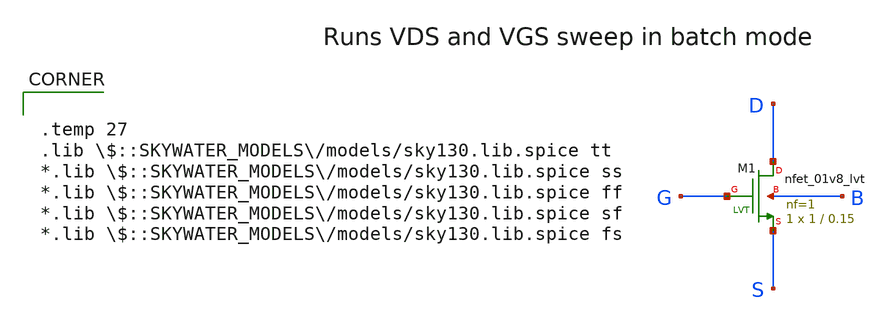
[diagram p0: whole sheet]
** sch_path: nmos_tb.sch
**.subckt nmos_tb
XM1 D G S B sky130_fd_pr__nfet_01v8_lvt L=0.15 W=1 nf=1 ad='int((nf+1)/2) * W/nf * 0.29' as='int((nf+2)/2) * W/nf * 0.29'
+ pd='2*int((nf+1)/2) * (W/nf + 0.29)' ps='2*int((nf+2)/2) * (W/nf + 0.29)' nrd='0.29 / W' nrs='0.29 / W'
+ sa=0 sb=0 sd=0 mult=1 m=1
**** begin user architecture code

.temp 27
.lib $::SKYWATER_MODELS/models/sky130.lib.spice tt
*.lib $::SKYWATER_MODELS/models/sky130.lib.spice ss
*.lib $::SKYWATER_MODELS/models/sky130.lib.spice ff
*.lib $::SKYWATER_MODELS/models/sky130.lib.spice sf
*.lib $::SKYWATER_MODELS/models/sky130.lib.spice fs



Vg G 0 1.8
Vs S 0 0
Vd D 0 1.8
Vb B 0 0

.control

save v(G) v(D) v(S) v(B)
save @m.xm1.msky130_fd_pr__nfet_01v8_lvt[gm]
save @m.xm1.msky130_fd_pr__nfet_01v8_lvt[gmbs]
save @m.xm1.msky130_fd_pr__nfet_01v8_lvt[gds]
save @m.xm1.msky130_fd_pr__nfet_01v8_lvt[vdsat]
save @m.xm1.msky130_fd_pr__nfet_01v8_lvt[vth]
save @m.xm1.msky130_fd_pr__nfet_01v8_lvt[id]
save @m.xm1.msky130_fd_pr__nfet_01v8_lvt[vbs]
save @m.xm1.msky130_fd_pr__nfet_01v8_lvt[vgs]
save @m.xm1.msky130_fd_pr__nfet_01v8_lvt[vds]
save @m.xm1.msky130_fd_pr__nfet_01v8_lvt[cgg]
save @m.xm1.msky130_fd_pr__nfet_01v8_lvt[cgs]
save @m.xm1.msky130_fd_pr__nfet_01v8_lvt[cgd]
save @m.xm1.msky130_fd_pr__nfet_01v8_lvt[cbg]
save @m.xm1.msky130_fd_pr__nfet_01v8_lvt[cbd]
save @m.xm1.msky130_fd_pr__nfet_01v8_lvt[cbs]
save @m.xm1.msky130_fd_pr__nfet_01v8_lvt[cdg]
save @m.xm1.msky130_fd_pr__nfet_01v8_lvt[cdd]
save @m.xm1.msky130_fd_pr__nfet_01v8_lvt[cds]
save @m.xm1.msky130_fd_pr__nfet_01v8_lvt[csg]
save @m.xm1.msky130_fd_pr__nfet_01v8_lvt[csd]
save @m.xm1.msky130_fd_pr__nfet_01v8_lvt[css]
save @m.xm1.msky130_fd_pr__nfet_01v8_lvt[cgb]
save @m.xm1.msky130_fd_pr__nfet_01v8_lvt[cdb]
save @m.xm1.msky130_fd_pr__nfet_01v8_lvt[csb]
save @m.xm1.msky130_fd_pr__nfet_01v8_lvt[cbb]
save @m.xm1.msky130_fd_pr__nfet_01v8_lvt[capbd]
save @m.xm1.msky130_fd_pr__nfet_01v8_lvt[capbs]

*dc Vd 0 1.8 0.1
dc Vd 0 1.8 0.3 Vg 0 1.8 0.3
reshape all [7] ;same value as second sweep length

plot @m.xm1.msky130_fd_pr__nfet_01v8_lvt[id] vs v(d) title 'id vs vd'
plot @m.xm1.msky130_fd_pr__nfet_01v8_lvt[gds] vs v(d) ylog title 'gds vs vd'

set hcopypscolor=1 ;colorful plots
hardcopy id_vd.ps @m.xm1.msky130_fd_pr__nfet_01v8_lvt[id] vs v(d) title 'id vs vd'
hardcopy gds_vd.ps @m.xm1.msky130_fd_pr__nfet_01v8_lvt[gds] vs v(d) ylog title 'gds vs vd'

.endc


**** end user architecture code
**.ends
.end
